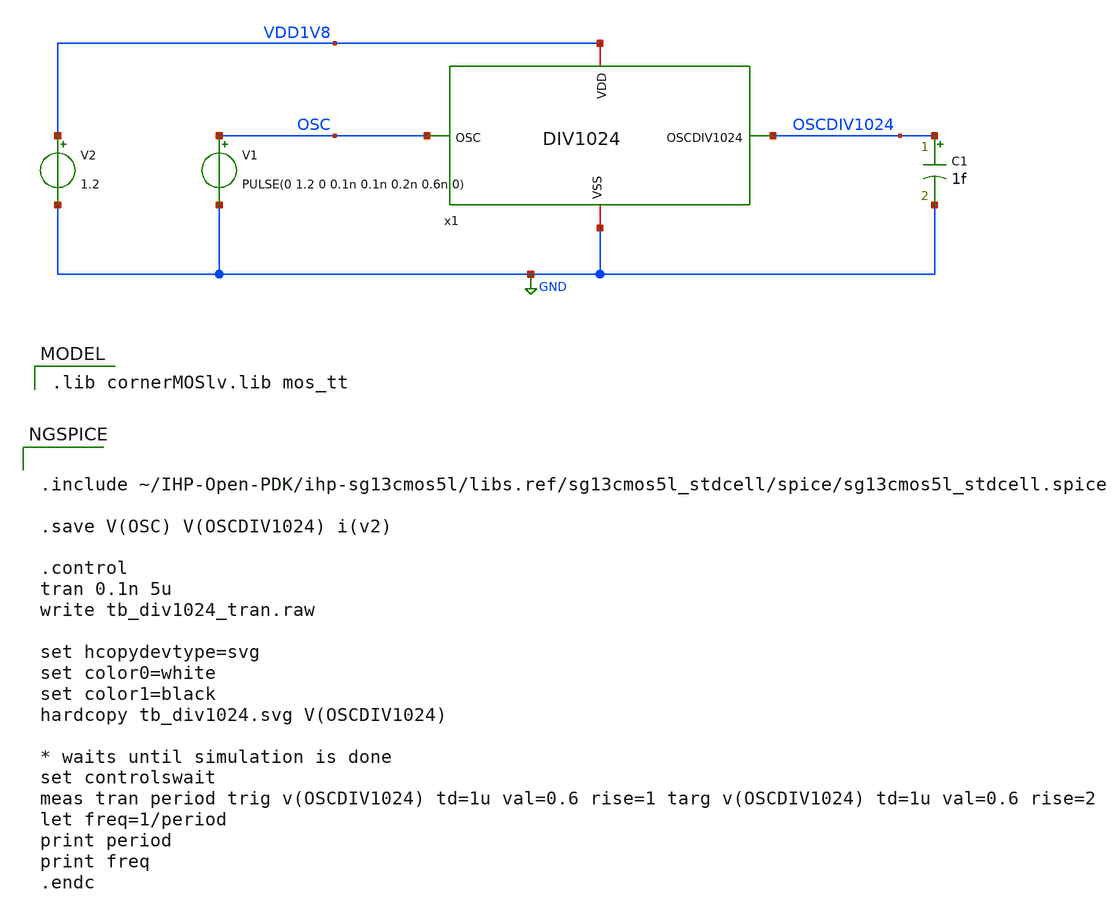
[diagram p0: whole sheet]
** sch_path: MPU9547-main/analog/schematic/tb_DIV1024_tran.sch
**.subckt tb_DIV1024_tran
V1 OSC GND PULSE(0 1.2 0 0.1n 0.1n 0.2n 0.6n 0)
V2 VDD1V8 GND 1.2
C1 OSCDIV1024 GND 1f m=1
x1 VDD1V8 GND OSCDIV1024 OSC DIV1024
**** begin user architecture code
 .lib cornerMOSlv.lib mos_tt



.include ~/IHP-Open-PDK/ihp-sg13cmos5l/libs.ref/sg13cmos5l_stdcell/spice/sg13cmos5l_stdcell.spice

.save V(OSC) V(OSCDIV1024) i(v2)

.control
tran 0.1n 5u
write tb_div1024_tran.raw

set hcopydevtype=svg
set color0=white
set color1=black
hardcopy tb_div1024.svg V(OSCDIV1024)

* waits until simulation is done
set controlswait
meas tran period trig v(OSCDIV1024) td=1u val=0.6 rise=1 targ v(OSCDIV1024) td=1u val=0.6 rise=2
let freq=1/period
print period
print freq
.endc


**** end user architecture code
**.ends

* expanding   symbol:  DIV1024.sym # of pins=4
** sym_path: MPU9547-main/analog/schematic/DIV1024.sym
** sch_path: MPU9547-main/analog/schematic/DIV1024.sch
.subckt DIV1024 VDD VSS OSCDIV1024 OSC
*.iopin VDD
*.iopin VSS
*.ipin OSC
*.opin OSCDIV1024
x23 net5 net2 OSC net2 net1 VDD VSS sg13cmos5l_dfrbp_1
x1 net8 net4 net5 net4 net3 VDD VSS sg13cmos5l_dfrbp_1
x2 net11 net7 net8 net7 net6 VDD VSS sg13cmos5l_dfrbp_1
x3 net14 net10 net11 net10 net9 VDD VSS sg13cmos5l_dfrbp_1
x4 net17 net13 net14 net13 net12 VDD VSS sg13cmos5l_dfrbp_1
x5 net20 net16 net17 net16 net15 VDD VSS sg13cmos5l_dfrbp_1
x6 net23 net19 net20 net19 net18 VDD VSS sg13cmos5l_dfrbp_1
x7 net26 net22 net23 net22 net21 VDD VSS sg13cmos5l_dfrbp_1
x8 net29 net25 net26 net25 net24 VDD VSS sg13cmos5l_dfrbp_1
x9 OSCDIV1024 net28 net29 net28 net27 VDD VSS sg13cmos5l_dfrbp_1
x11 net1 VDD VSS sg13cmos5l_tiehi
x12 net3 VDD VSS sg13cmos5l_tiehi
x13 net6 VDD VSS sg13cmos5l_tiehi
x14 net9 VDD VSS sg13cmos5l_tiehi
x15 net12 VDD VSS sg13cmos5l_tiehi
x16 net15 VDD VSS sg13cmos5l_tiehi
x17 net18 VDD VSS sg13cmos5l_tiehi
x18 net21 VDD VSS sg13cmos5l_tiehi
x19 net24 VDD VSS sg13cmos5l_tiehi
x20 net27 VDD VSS sg13cmos5l_tiehi
x10 net32 net33 net31 net31 net31 VDD VSS sg13cmos5l_dfrbp_1
x21 net34 net35 net30 net30 net30 VDD VSS sg13cmos5l_dfrbp_1
x22 net30 VDD VSS sg13cmos5l_tielo
x24 net31 VDD VSS sg13cmos5l_tielo
* noconn #net34
* noconn #net35
* noconn #net32
* noconn #net33
x25 VSS VDD VSS sg13cmos5l_tielo
x26 VSS VDD VSS sg13cmos5l_tielo
x27 VSS VDD VSS sg13cmos5l_tielo
.ends

.GLOBAL GND
.end
